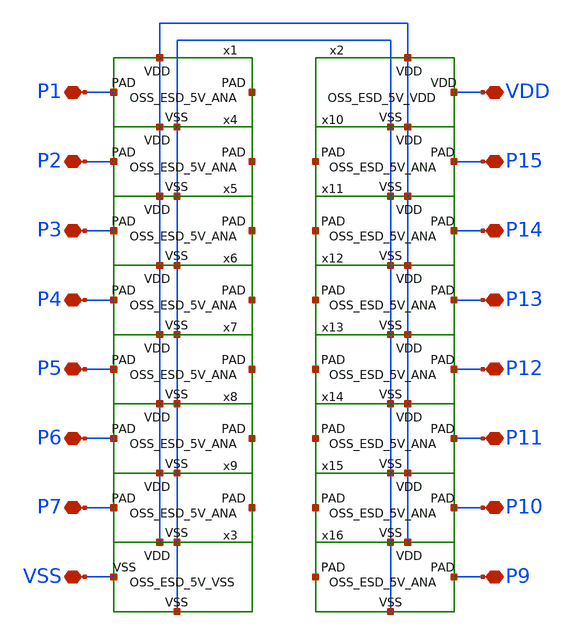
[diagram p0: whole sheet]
** sch_path: libs.tech/xschem/TR-1um_frame/OSS_FRAME.sch
**.subckt OSS_FRAME P1 P2 P3 P4 P5 P6 P7 VSS VDD P15 P14 P13 P12 P11 P10 P9
*.iopin P1
*.iopin P2
*.iopin P3
*.iopin P4
*.iopin P5
*.iopin P6
*.iopin P7
*.iopin VSS
*.iopin VDD
*.iopin P15
*.iopin P14
*.iopin P13
*.iopin P12
*.iopin P11
*.iopin P10
*.iopin P9
x1 VDD P1 VSS OSS_ESD_5V_ANA
x2 VDD VSS OSS_ESD_5V_VDD
x3 VDD VSS OSS_ESD_5V_VSS
x4 VDD P2 VSS OSS_ESD_5V_ANA
x5 VDD P3 VSS OSS_ESD_5V_ANA
x6 VDD P4 VSS OSS_ESD_5V_ANA
x7 VDD P5 VSS OSS_ESD_5V_ANA
x8 VDD P6 VSS OSS_ESD_5V_ANA
x9 VDD P7 VSS OSS_ESD_5V_ANA
x10 VDD P15 VSS OSS_ESD_5V_ANA
x11 VDD P14 VSS OSS_ESD_5V_ANA
x12 VDD P13 VSS OSS_ESD_5V_ANA
x13 VDD P12 VSS OSS_ESD_5V_ANA
x14 VDD P11 VSS OSS_ESD_5V_ANA
x15 VDD P10 VSS OSS_ESD_5V_ANA
x16 VDD P9 VSS OSS_ESD_5V_ANA
**.ends

* expanding   symbol:  OSS_ESD_5V_ANA.sym # of pins=4
** sym_path: libs.tech/xschem/TR-1um_frame/OSS_ESD_5V_ANA.sym
** sch_path: libs.tech/xschem/TR-1um_frame/OSS_ESD_5V_ANA.sch
.subckt OSS_ESD_5V_ANA VDD PAD VSS
*.iopin PAD
*.iopin VDD
*.iopin VSS
XXM1 PAD VDD VDD VDD MPE w=500u l=2u as=0 ad=0 ps=0 pd=0 nrd=0 nrs=0 m=1
XXM2 PAD VSS VSS VSS MNE w=500u l=2u as=0 ad=0 ps=0 pd=0 nrd=0 nrs=0 m=1
.ends


* expanding   symbol:  OSS_ESD_5V_VDD.sym # of pins=3
** sym_path: libs.tech/xschem/TR-1um_frame/OSS_ESD_5V_VDD.sym
** sch_path: libs.tech/xschem/TR-1um_frame/OSS_ESD_5V_VDD.sch
.subckt OSS_ESD_5V_VDD VDD VSS
*.iopin VDD
*.iopin VSS
XXM1 VDD VDD VDD VDD MPE w=500u l=2u as=0 ad=0 ps=0 pd=0 nrd=0 nrs=0 m=1
XXM2 VDD VSS VSS VSS MNE w=500u l=2u as=0 ad=0 ps=0 pd=0 nrd=0 nrs=0 m=1
.ends


* expanding   symbol:  OSS_ESD_5V_VSS.sym # of pins=3
** sym_path: libs.tech/xschem/TR-1um_frame/OSS_ESD_5V_VSS.sym
** sch_path: libs.tech/xschem/TR-1um_frame/OSS_ESD_5V_VSS.sch
.subckt OSS_ESD_5V_VSS VDD VSS
*.iopin VSS
*.iopin VDD
XXM1 VSS VDD VDD VDD MPE w=500u l=2u as=0 ad=0 ps=0 pd=0 nrd=0 nrs=0 m=1
XXM2 VSS VSS VSS VSS MNE w=500u l=2u as=0 ad=0 ps=0 pd=0 nrd=0 nrs=0 m=1
.ends

.end
